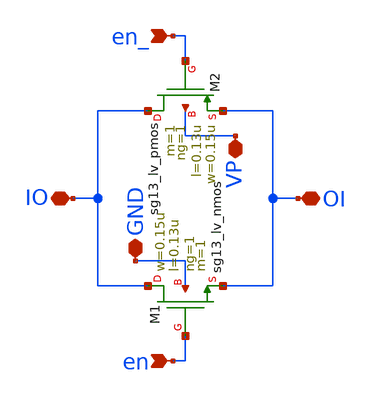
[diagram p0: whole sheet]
** sch_path: PLL0663-main/schematic/xschem/divider/passgate_scaled.sch
**.subckt passgate_scaled OI IO VP GND en_ en
*.iopin OI
*.iopin IO
*.iopin VP
*.iopin GND
*.ipin en_
*.ipin en
XM1 IO en OI GND sg13_lv_nmos w=0.15u l=0.13u ng=1 m=1 mm_ok=1
XM2 IO en_ OI VP sg13_lv_pmos w=0.15u l=0.13u ng=1 m=1 mm_ok=1
**.ends
.end
